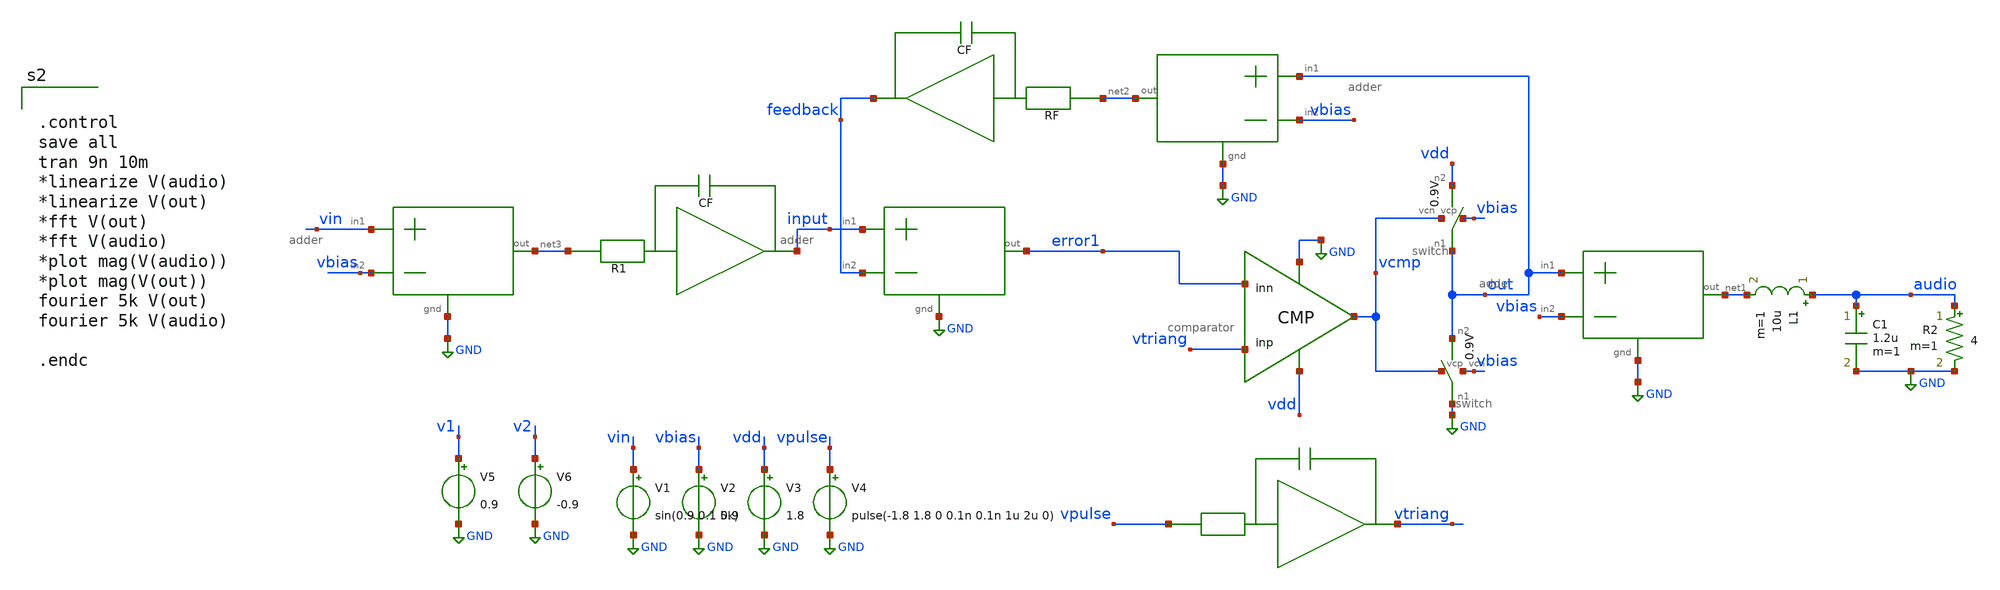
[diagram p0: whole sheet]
** sch_path: xschem/src/behavior_mdl/behavior_mdl.sch
**.subckt behavior_mdl
x2 vtriang error1 vcmp vdd GND comparator
V2 vbias GND 0.9
V3 vdd GND 1.8
V4 vpulse GND pulse(-1.8 1.8 0 0.1n 0.1n 1u 2u 0)
V1 vin GND sin(0.9 0.1 5k)
x1 GND out vcmp vbias switch
x3 out vdd vbias vcmp switch
x4 net2 feedback integrator_feedback
x5 net3 input integrator_input
x6 input feedback error1 GND adder
x7 vpulse vtriang triang
L1 audio net1 10u m=1
C1 audio GND 1.2u m=1
R2 audio GND 4 m=1
V5 v1 GND 0.9
V6 v2 GND -0.9
x8 out vbias net2 GND adder
x9 vin vbias net3 GND adder
x10 out vbias net1 GND adder
**** begin user architecture code


.include /home/eda/xschem/xschem_library/src/behavior_mdl/OTA.spice
.include /home/eda/xschem/xschem_library/src/behavior_mdl/comparator.spice
.include /home/eda/xschem/xschem_library/src/behavior_mdl/switch.spice
.include /home/eda/xschem/xschem_library/src/behavior_mdl/integrator_feedback.spice
.include /home/eda/xschem/xschem_library/src/behavior_mdl/integrator_input.spice
.include /home/eda/xschem/xschem_library/src/behavior_mdl/adder.spice
.include /home/eda/xschem/xschem_library/src/behavior_mdl/triang.spice
.include /home/eda/xschem/xschem_library/src/behavior_mdl/ideal_amp.spice




.control
save all
tran 9n 10m
*linearize V(audio)
*linearize V(out)
*fft V(out)
*fft V(audio)
*plot mag(V(audio))
*plot mag(V(out))
fourier 5k V(out)
fourier 5k V(audio)

.endc




**** end user architecture code
**.ends
.GLOBAL GND
.end
